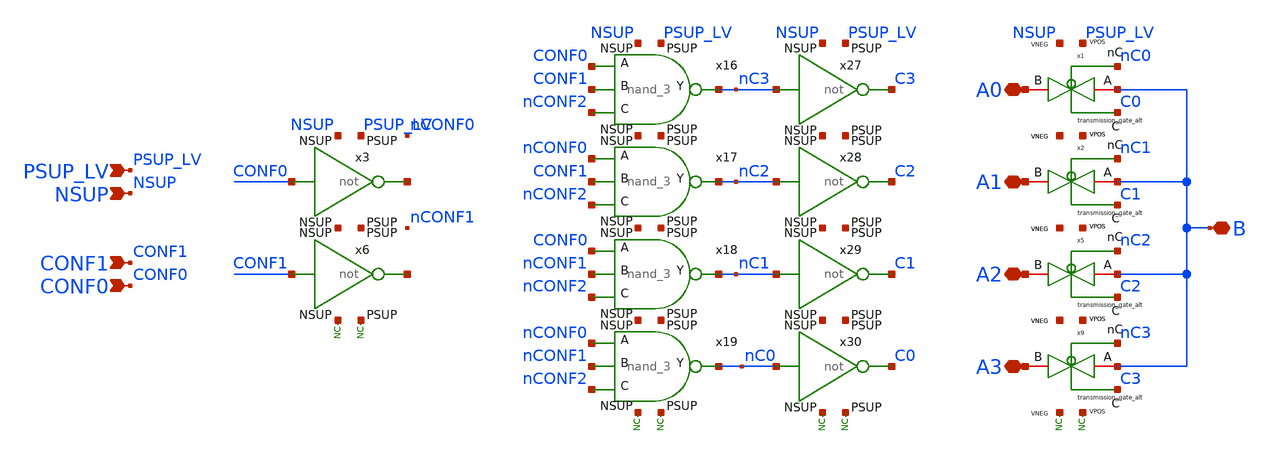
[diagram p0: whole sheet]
** sch_path: xschem/blocks/mux_2/mux_2.sch
**.subckt mux_2 PSUP_LV NSUP CONF1 CONF0 A0 A1 A2 A3 B
*.ipin PSUP_LV
*.ipin NSUP
*.ipin CONF1
*.ipin CONF0
*.iopin A0
*.iopin A1
*.iopin A2
*.iopin A3
*.iopin B
x16 nC3 CONF0 nCONF2 PSUP_LV NSUP CONF1 nand_3
x17 nC2 nCONF0 nCONF2 PSUP_LV NSUP CONF1 nand_3
x18 nC1 CONF0 nCONF2 PSUP_LV NSUP nCONF1 nand_3
x19 nC0 nCONF0 nCONF2 PSUP_LV NSUP nCONF1 nand_3
* noconn NSUP
* noconn PSUP_LV
* noconn NSUP
* noconn PSUP_LV
x27 PSUP_LV nC3 C3 NSUP not
x28 PSUP_LV nC2 C2 NSUP not
x29 PSUP_LV nC1 C1 NSUP not
x30 PSUP_LV nC0 C0 NSUP not
* noconn NSUP
* noconn PSUP_LV
x3 PSUP_LV CONF0 net1 NSUP not
x6 PSUP_LV CONF1 net2 NSUP not
x1 C0 B A0 nC0 PSUP_LV NSUP transmission_gate_alt
x2 C1 B A1 nC1 PSUP_LV NSUP transmission_gate_alt
x5 C2 B A2 nC2 PSUP_LV NSUP transmission_gate_alt
x9 C3 B A3 nC3 PSUP_LV NSUP transmission_gate_alt
* noconn NSUP
* noconn PSUP_LV
**.ends

* expanding   symbol:  blocks/nand_3/nand_3.sym # of pins=8
** sym_path: xschem/blocks/nand_3/nand_3.sym
** sch_path: xschem/blocks/nand_3/nand_3.sch
.subckt nand_3 Y A C PSUP NSUP B
*.ipin PSUP
*.ipin NSUP
*.ipin A
*.ipin B
*.opin Y
*.ipin C
XM5 net1 C NSUP NSUP nfet_03v3 L=0.28u W=0.22u nf=1 ad='int((nf+1)/2) * W/nf * 0.18u' as='int((nf+2)/2) * W/nf * 0.18u'
+ pd='2*int((nf+1)/2) * (W/nf + 0.18u)' ps='2*int((nf+2)/2) * (W/nf + 0.18u)' nrd='0.18u / W' nrs='0.18u / W'
+ sa=0 sb=0 sd=0 m=1
XM1 Y A net2 NSUP nfet_03v3 L=0.28u W=0.22u nf=1 ad='int((nf+1)/2) * W/nf * 0.18u' as='int((nf+2)/2) * W/nf * 0.18u'
+ pd='2*int((nf+1)/2) * (W/nf + 0.18u)' ps='2*int((nf+2)/2) * (W/nf + 0.18u)' nrd='0.18u / W' nrs='0.18u / W'
+ sa=0 sb=0 sd=0 m=1
XM2 Y C PSUP PSUP pfet_03v3 L=0.28u W=0.5u nf=1 ad='int((nf+1)/2) * W/nf * 0.18u' as='int((nf+2)/2) * W/nf * 0.18u'
+ pd='2*int((nf+1)/2) * (W/nf + 0.18u)' ps='2*int((nf+2)/2) * (W/nf + 0.18u)' nrd='0.18u / W' nrs='0.18u / W'
+ sa=0 sb=0 sd=0 m=1
XM3 Y B PSUP PSUP pfet_03v3 L=0.28u W=0.5u nf=1 ad='int((nf+1)/2) * W/nf * 0.18u' as='int((nf+2)/2) * W/nf * 0.18u'
+ pd='2*int((nf+1)/2) * (W/nf + 0.18u)' ps='2*int((nf+2)/2) * (W/nf + 0.18u)' nrd='0.18u / W' nrs='0.18u / W'
+ sa=0 sb=0 sd=0 m=1
XM4 net2 B net1 NSUP nfet_03v3 L=0.28u W=0.22u nf=1 ad='int((nf+1)/2) * W/nf * 0.18u' as='int((nf+2)/2) * W/nf * 0.18u'
+ pd='2*int((nf+1)/2) * (W/nf + 0.18u)' ps='2*int((nf+2)/2) * (W/nf + 0.18u)' nrd='0.18u / W' nrs='0.18u / W'
+ sa=0 sb=0 sd=0 m=1
XM6 Y A PSUP PSUP pfet_03v3 L=0.28u W=0.5u nf=1 ad='int((nf+1)/2) * W/nf * 0.18u' as='int((nf+2)/2) * W/nf * 0.18u'
+ pd='2*int((nf+1)/2) * (W/nf + 0.18u)' ps='2*int((nf+2)/2) * (W/nf + 0.18u)' nrd='0.18u / W' nrs='0.18u / W'
+ sa=0 sb=0 sd=0 m=1
.ends


* expanding   symbol:  blocks/not/not.sym # of pins=6
** sym_path: xschem/blocks/not/not.sym
** sch_path: xschem/blocks/not/not.sch
.subckt not PSUP A B NSUP
*.ipin PSUP
*.ipin NSUP
*.ipin A
*.opin B
XM2 B A NSUP NSUP nfet_03v3 L=0.28u W=0.22u nf=1 ad='int((nf+1)/2) * W/nf * 0.18u' as='int((nf+2)/2) * W/nf * 0.18u'
+ pd='2*int((nf+1)/2) * (W/nf + 0.18u)' ps='2*int((nf+2)/2) * (W/nf + 0.18u)' nrd='0.18u / W' nrs='0.18u / W'
+ sa=0 sb=0 sd=0 m=1
XM1 B A PSUP PSUP pfet_03v3 L=0.28u W=0.5u nf=1 ad='int((nf+1)/2) * W/nf * 0.18u' as='int((nf+2)/2) * W/nf * 0.18u'
+ pd='2*int((nf+1)/2) * (W/nf + 0.18u)' ps='2*int((nf+2)/2) * (W/nf + 0.18u)' nrd='0.18u / W' nrs='0.18u / W'
+ sa=0 sb=0 sd=0 m=1
.ends


* expanding   symbol:  blocks/transmission_gate/transmission_gate_alt.sym # of pins=8
** sym_path: xschem/blocks/transmission_gate/transmission_gate_alt.sym
** sch_path: xschem/blocks/transmission_gate/transmission_gate_alt.sch
.subckt transmission_gate_alt C A B nC VPOS VNEG
*.iopin A
*.iopin B
*.ipin C
*.ipin nC
*.ipin VPOS
*.ipin VNEG
x1 C A B nC VPOS VNEG transmission_gate
.ends


* expanding   symbol:  blocks/transmission_gate/transmission_gate.sym # of pins=6
** sym_path: xschem/blocks/transmission_gate/transmission_gate.sym
** sch_path: xschem/blocks/transmission_gate/transmission_gate.sch
.subckt transmission_gate C A B nC VPOS VNEG
*.iopin A
*.iopin B
*.ipin C
*.ipin nC
*.ipin VPOS
*.ipin VNEG
XM3 A C B VNEG nfet_03v3 L=2u W=10u nf=1 ad='int((nf+1)/2) * W/nf * 0.18u' as='int((nf+2)/2) * W/nf * 0.18u'
+ pd='2*int((nf+1)/2) * (W/nf + 0.18u)' ps='2*int((nf+2)/2) * (W/nf + 0.18u)' nrd='0.18u / W' nrs='0.18u / W'
+ sa=0 sb=0 sd=0 m=2
XM4 A nC B VPOS pfet_03v3 L=2u W=10u nf=1 ad='int((nf+1)/2) * W/nf * 0.18u' as='int((nf+2)/2) * W/nf * 0.18u'
+ pd='2*int((nf+1)/2) * (W/nf + 0.18u)' ps='2*int((nf+2)/2) * (W/nf + 0.18u)' nrd='0.18u / W' nrs='0.18u / W'
+ sa=0 sb=0 sd=0 m=4
.ends

.end
